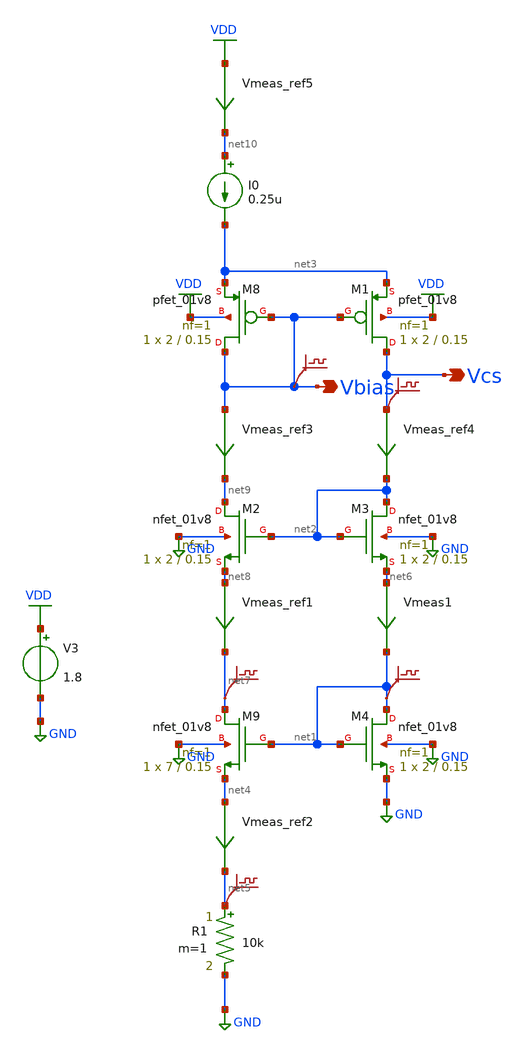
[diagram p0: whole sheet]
** sch_path: lib/xschem/LDO/casc_mirror.sch
**.subckt casc_mirror Vbias Vcs
*.opin Vbias
*.opin Vcs
XM8 Vbias Vbias net3 VDD sky130_fd_pr__pfet_01v8 L=0.15 W=2 nf=1 ad='int((nf+1)/2) * W/nf * 0.29' as='int((nf+2)/2) * W/nf * 0.29'
+ pd='2*int((nf+1)/2) * (W/nf + 0.29)' ps='2*int((nf+2)/2) * (W/nf + 0.29)' nrd='0.29 / W' nrs='0.29 / W'
+ sa=0 sb=0 sd=0 mult=1 m=1
XM9 net7 net1 net4 GND sky130_fd_pr__nfet_01v8 L=0.15 W=7 nf=1 ad='int((nf+1)/2) * W/nf * 0.29' as='int((nf+2)/2) * W/nf * 0.29'
+ pd='2*int((nf+1)/2) * (W/nf + 0.29)' ps='2*int((nf+2)/2) * (W/nf + 0.29)' nrd='0.29 / W' nrs='0.29 / W'
+ sa=0 sb=0 sd=0 mult=1 m=1
XM1 Vcs Vbias net3 VDD sky130_fd_pr__pfet_01v8 L=0.15 W=2 nf=1 ad='int((nf+1)/2) * W/nf * 0.29' as='int((nf+2)/2) * W/nf * 0.29'
+ pd='2*int((nf+1)/2) * (W/nf + 0.29)' ps='2*int((nf+2)/2) * (W/nf + 0.29)' nrd='0.29 / W' nrs='0.29 / W'
+ sa=0 sb=0 sd=0 mult=1 m=1
XM2 net9 net2 net8 GND sky130_fd_pr__nfet_01v8 L=0.15 W=2 nf=1 ad='int((nf+1)/2) * W/nf * 0.29' as='int((nf+2)/2) * W/nf * 0.29'
+ pd='2*int((nf+1)/2) * (W/nf + 0.29)' ps='2*int((nf+2)/2) * (W/nf + 0.29)' nrd='0.29 / W' nrs='0.29 / W'
+ sa=0 sb=0 sd=0 mult=1 m=1
XM3 net2 net2 net6 GND sky130_fd_pr__nfet_01v8 L=0.15 W=2 nf=1 ad='int((nf+1)/2) * W/nf * 0.29' as='int((nf+2)/2) * W/nf * 0.29'
+ pd='2*int((nf+1)/2) * (W/nf + 0.29)' ps='2*int((nf+2)/2) * (W/nf + 0.29)' nrd='0.29 / W' nrs='0.29 / W'
+ sa=0 sb=0 sd=0 mult=1 m=1
XM4 net1 net1 GND GND sky130_fd_pr__nfet_01v8 L=0.15 W=2 nf=1 ad='int((nf+1)/2) * W/nf * 0.29' as='int((nf+2)/2) * W/nf * 0.29'
+ pd='2*int((nf+1)/2) * (W/nf + 0.29)' ps='2*int((nf+2)/2) * (W/nf + 0.29)' nrd='0.29 / W' nrs='0.29 / W'
+ sa=0 sb=0 sd=0 mult=1 m=1
R1 net5 GND 10k m=1
Vmeas_ref2 net4 net5 0
.save i(vmeas_ref2)
Vmeas1 net6 net1 0
.save i(vmeas1)
Vmeas_ref1 net8 net7 0
.save i(vmeas_ref1)
.save v(net7)
.save v(net5)
.save v(net1)
Vmeas_ref3 Vbias net9 0
.save i(vmeas_ref3)
Vmeas_ref4 Vcs net2 0
.save i(vmeas_ref4)
V3 VDD GND 1.8
Vmeas_ref5 VDD net10 0
.save i(vmeas_ref5)
I0 net10 net3 0.25u
.save v(vbias)
.save v(vcs)
**** begin user architecture code

.lib $::SKYWATER_MODELS/sky130.lib.spice tt


**** end user architecture code
**.ends
.GLOBAL VDD
.GLOBAL GND
**** begin user architecture code



.control
save all
op
write casc_mirror.raw
.endc


**** end user architecture code
.end
